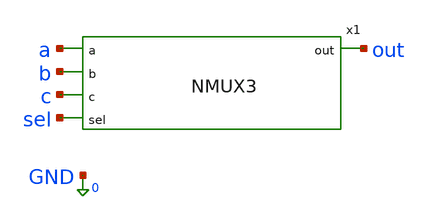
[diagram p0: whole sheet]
** sch_path: xschem_designs/NMUX3_TB.sch
**.subckt NMUX3_TB
x1 out a b c sel NMUX3
**** begin user architecture code


.global VDD GND BP BN
.option temp=27
.include /usr/local/share/pdk/gf180mcuC/libs.tech/ngspice/design.ngspice
.lib /usr/local/share/pdk/gf180mcuC/libs.tech/ngspice/sm141064.ngspice typical

Vdd VDD 0 3.3
Vbp BP VDD 2.7
Vbn BN GND -2.7
Va a 0 PWL(0 0 89.9n 0 90.1n 1.4 179.9n 1.4 180.1n 3.3 269.9n 3.3 r=0)
Vb b 0 PWL(0 0 269.9n 0 270.1n 1.4 539.9n 1.4 540.1n 3.3  809.9n 3.3 r=0)
Vc c 0 PWL(0 0 809.9n  0 810.1n 1.4 1619.9n 1.4 1620.1n 3.3 2429.9n 3.3 r=0)
Vd sel 0 PWL(0 0 2429.9n 0 2430.1n 1.4 4859.9n 1.4 4860.1n 3.3 7289.9n 3.3)

.control
  save all
  tran 0.1n 7289.9n
  write MUX3_TB.raw
.endc
.end


**** end user architecture code
**.ends
.end
